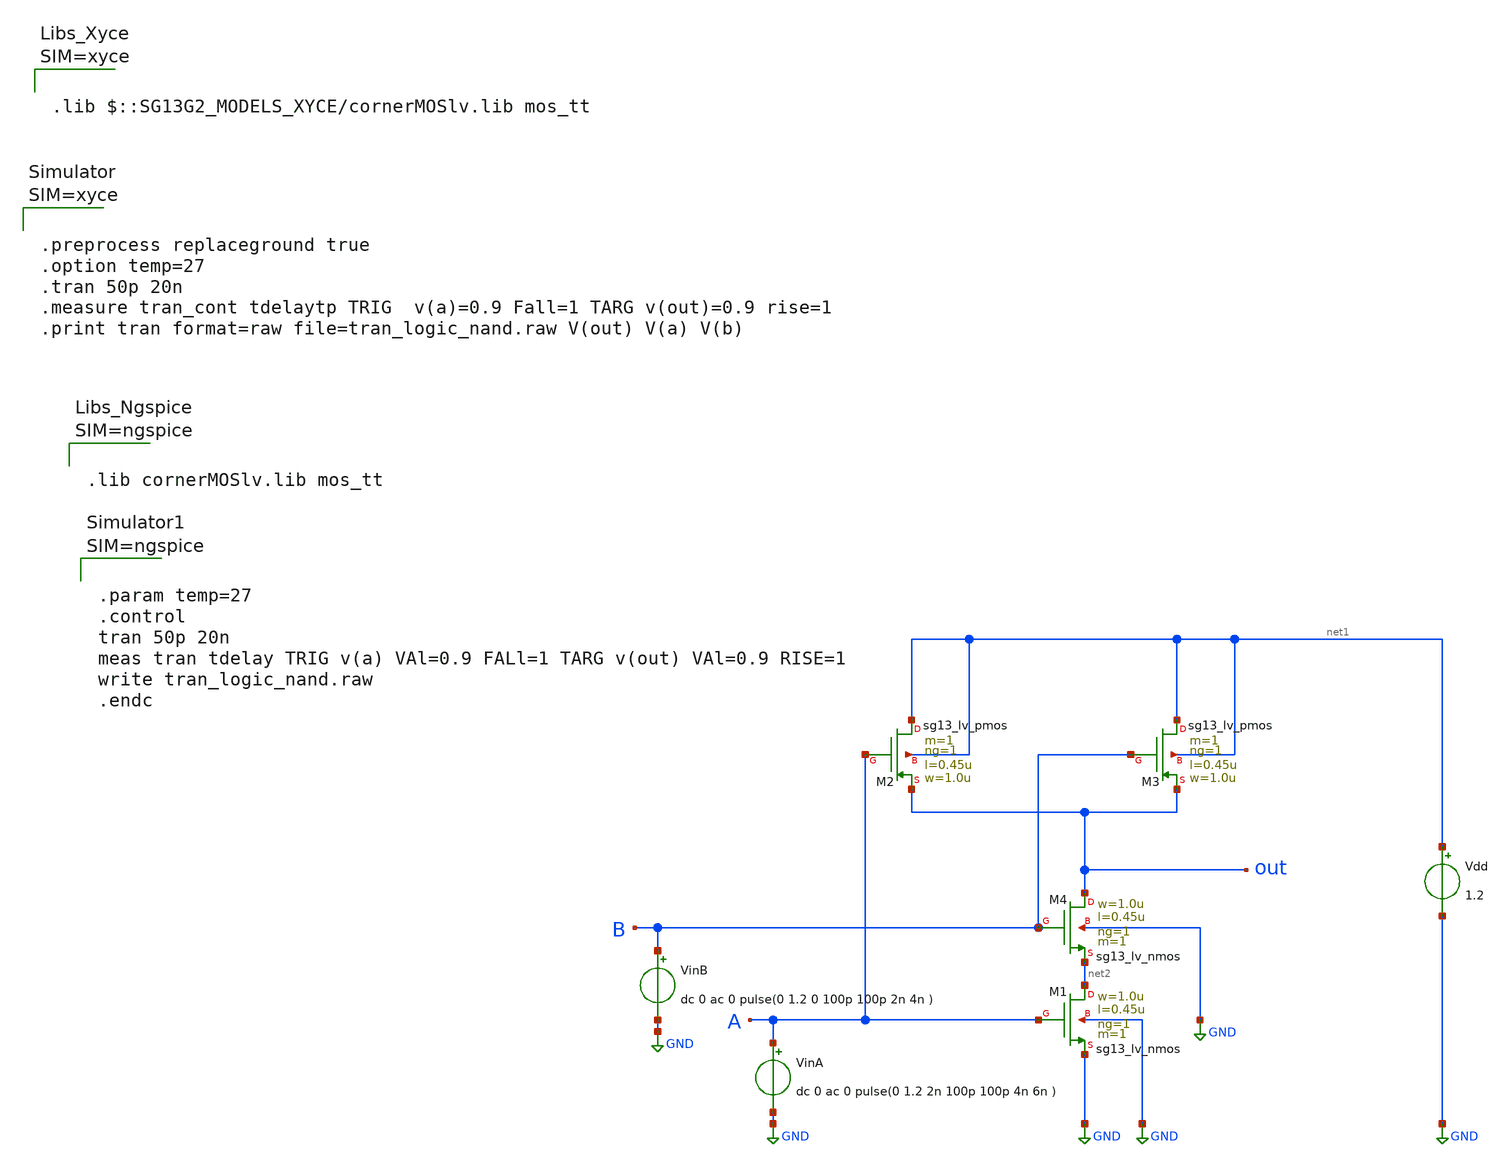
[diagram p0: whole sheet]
** sch_path: ihp-sg13g2/libs.tech/xschem/sg13g2_tests_xyce/tran_logic_nand.sch
* Copyright 2023 IHP PDK Authors
**.subckt tran_logic_nand
VinA A GND dc 0 ac 0 pulse(0 1.2 2n 100p 100p 4n 6n )
Vdd net1 GND 1.2
XM1 net2 A GND GND sg13_lv_nmos w=1.0u l=0.45u ng=1 m=1 mm_ok=1
XM2 net1 A out net1 sg13_lv_pmos w=1.0u l=0.45u ng=1 m=1 mm_ok=1
XM3 net1 B out net1 sg13_lv_pmos w=1.0u l=0.45u ng=1 m=1 mm_ok=1
XM4 out B net2 GND sg13_lv_nmos w=1.0u l=0.45u ng=1 m=1 mm_ok=1
VinB B GND dc 0 ac 0 pulse(0 1.2 0 100p 100p 2n 4n )
**** begin user architecture code









.lib cornerMOSlv.lib mos_tt






.param temp=27
.control
tran 50p 20n
meas tran tdelay TRIG v(a) VAl=0.9 FALl=1 TARG v(out) VAl=0.9 RISE=1
write tran_logic_nand.raw
.endc



**** end user architecture code
**.ends
.GLOBAL GND
.end
